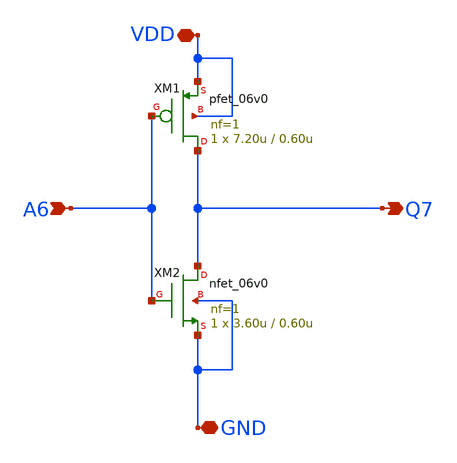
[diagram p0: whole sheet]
** sch_path: member_project/noritsuna/inverter/xschem/inverter_circit_only.sch
**.subckt inverter_circit_only A6 Q7 VDD GND
*.ipin A6
*.opin Q7
*.iopin VDD
*.iopin GND
XM1 Q7 A6 VDD VDD pfet_06v0 L=0.60u W=7.20u nf=1 ad='int((nf+1)/2) * W/nf * 0.18u' as='int((nf+2)/2) * W/nf * 0.18u'
+ pd='2*int((nf+1)/2) * (W/nf + 0.18u)' ps='2*int((nf+2)/2) * (W/nf + 0.18u)' nrd='0.18u / W' nrs='0.18u / W'
+ sa=0 sb=0 sd=0 m=1
XM2 Q7 A6 GND GND nfet_06v0 L=0.60u W=3.60u nf=1 ad='int((nf+1)/2) * W/nf * 0.18u' as='int((nf+2)/2) * W/nf * 0.18u'
+ pd='2*int((nf+1)/2) * (W/nf + 0.18u)' ps='2*int((nf+2)/2) * (W/nf + 0.18u)' nrd='0.18u / W' nrs='0.18u / W'
+ sa=0 sb=0 sd=0 m=1
**.ends
.end
